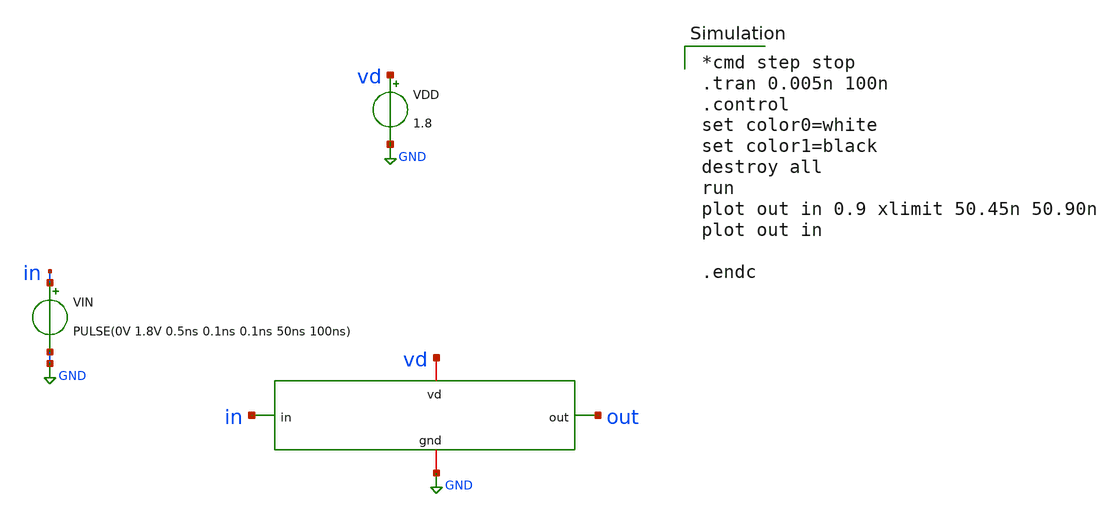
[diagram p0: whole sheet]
** sch_path: mag/sigma-delta_modulator/xschem/comp_tb-tran.sch
* Copyright 2020 Stefan Frederik Schippers
* Licensed under the Apache License, Version 2.0 (the "License");
* you may not use this file except in compliance with the License.
* You may obtain a copy of the License at
* https://www.apache.org/licenses/LICENSE-2.0
* Unless required by applicable law or agreed to in writing, software
* distributed under the License is distributed on an "AS IS" BASIS,
* WITHOUT WARRANTIES OR CONDITIONS OF ANY KIND, either express or implied.
* See the License for the specific language governing permissions and
* limitations under the License.
**.subckt comp_tb-tran
VIN in GND PULSE(0V 1.8V 0.5ns 0.1ns 0.1ns 50ns 100ns)
VDD vd GND 1.8
X1 vd out in GND comp
**** begin user architecture code

*cmd step stop
.tran 0.005n 100n
.control
set color0=white
set color1=black
destroy all
run
plot out in 0.9 xlimit 50.45n 50.90n
plot out in

.endc

 .lib $::SKYWATER_MODELS/sky130.lib.spice tt
.include $::SKYWATER_STDCELLS/sky130_fd_sc_hd.spice

**** end user architecture code
**.ends

* expanding   symbol:
*+  /home/hugodg/projects-sky130/temp-sensor/sigma-delta_modulator/xschem/comp.sym # of pins=4
** sym_path: mag/sigma-delta_modulator/xschem/comp.sym
** sch_path: mag/sigma-delta_modulator/xschem/comp.sch
.subckt comp vd out in gnd
*.ipin in
*.iopin gnd
*.opin out
*.iopin vd
**** begin user architecture code




**** end user architecture code
XN1 vd in out out sky130_fd_pr__nfet_01v8 L=0.15 W=4 nf=1 ad='int((nf+1)/2) * W/nf * 0.29' as='int((nf+2)/2) * W/nf * 0.29'
+ pd='2*int((nf+1)/2) * (W/nf + 0.29)' ps='2*int((nf+2)/2) * (W/nf + 0.29)' nrd='0.29 / W' nrs='0.29 / W'
+ sa=0 sb=0 sd=0 mult=1 m=1
XP1 gnd in out out sky130_fd_pr__pfet_01v8 L=0.15 W=1 nf=1 ad='int((nf+1)/2) * W/nf * 0.29' as='int((nf+2)/2) * W/nf * 0.29'
+ pd='2*int((nf+1)/2) * (W/nf + 0.29)' ps='2*int((nf+2)/2) * (W/nf + 0.29)' nrd='0.29 / W' nrs='0.29 / W'
+ sa=0 sb=0 sd=0 mult=1 m=1
.ends

.GLOBAL GND
.end
